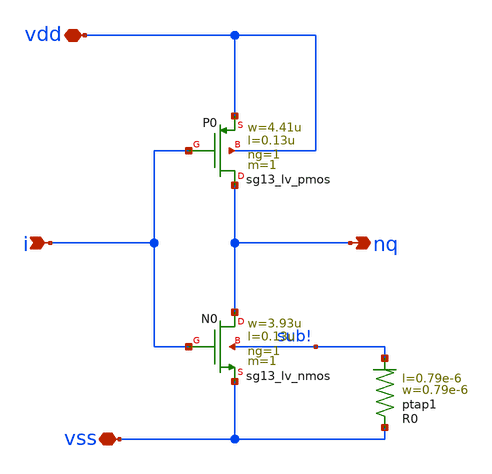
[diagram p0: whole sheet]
** sch_path: ihp-sg13g2/libs.ref/sg13g2_io/sch/xschem/sg13g2_io_inv_x1.sch
**.subckt sg13g2_io_inv_x1 vss i vdd nq
*.iopin vss
*.ipin i
*.iopin vdd
*.opin nq
XN0 nq i vss sub! sg13_lv_nmos w=3.93u l=0.13u ng=1 m=1 mm_ok=1
XP0 nq i vdd vdd sg13_lv_pmos w=4.41u l=0.13u ng=1 m=1 mm_ok=1
XR0 vss sub! ptap1 R=259 w=0.79e-6 l=0.79e-6
**.ends
.end
